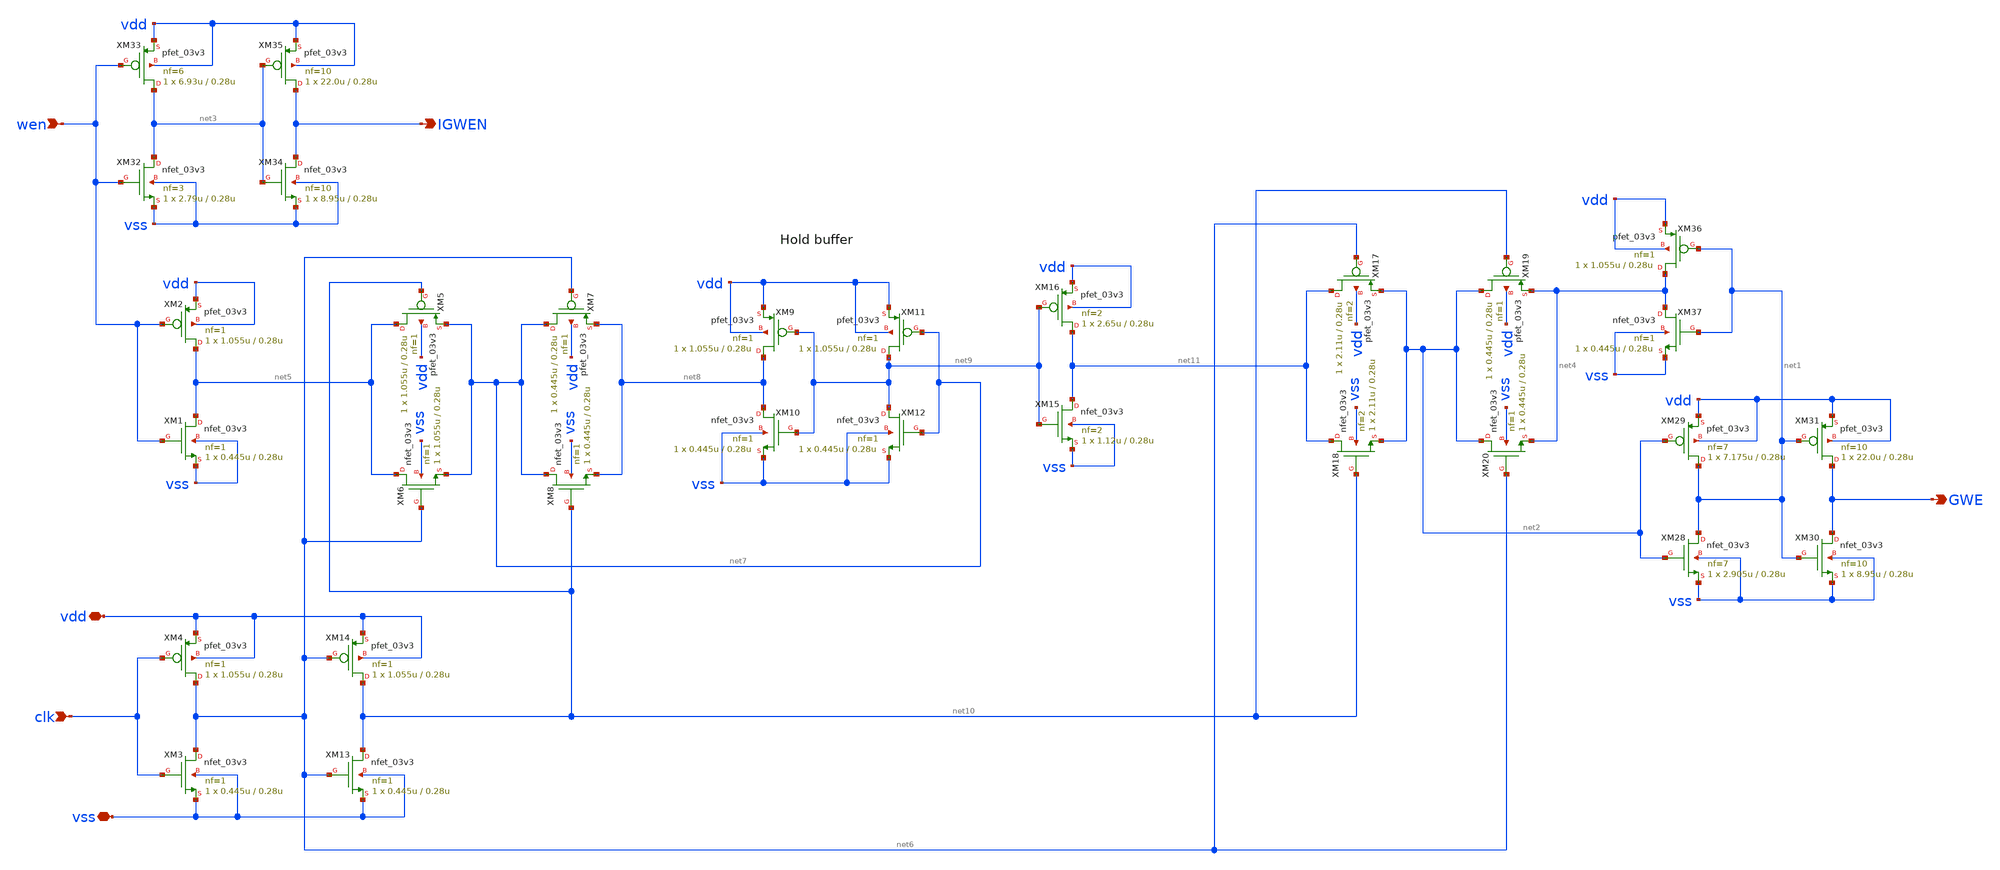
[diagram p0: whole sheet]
** sch_path: cells/gf180mcu_ocd_ip_sram__sram1024x8m8wm1/xschem/wen_v2_3v1024x8m81.sch
**.subckt wen_v2_3v1024x8m81 GWE wen IGWEN clk vdd vss
*.opin GWE
*.ipin wen
*.opin IGWEN
*.ipin clk
*.iopin vdd
*.iopin vss
XM28 net1 net2 vss vss nfet_03v3 L=0.28u W=2.905u nf=7 ad='int((nf+1)/2) * W/nf * 0.18u' as='int((nf+2)/2) * W/nf * 0.18u'
+ pd='2*int((nf+1)/2) * (W/nf + 0.18u)' ps='2*int((nf+2)/2) * (W/nf + 0.18u)' nrd='0.18u / W' nrs='0.18u / W'
+ sa=0 sb=0 sd=0 m=1
XM29 net1 net2 vdd vdd pfet_03v3 L=0.28u W=7.175u nf=7 ad='int((nf+1)/2) * W/nf * 0.18u' as='int((nf+2)/2) * W/nf * 0.18u'
+ pd='2*int((nf+1)/2) * (W/nf + 0.18u)' ps='2*int((nf+2)/2) * (W/nf + 0.18u)' nrd='0.18u / W' nrs='0.18u / W'
+ sa=0 sb=0 sd=0 m=1
XM30 GWE net1 vss vss nfet_03v3 L=0.28u W=8.95u nf=10 ad='int((nf+1)/2) * W/nf * 0.18u' as='int((nf+2)/2) * W/nf * 0.18u'
+ pd='2*int((nf+1)/2) * (W/nf + 0.18u)' ps='2*int((nf+2)/2) * (W/nf + 0.18u)' nrd='0.18u / W' nrs='0.18u / W'
+ sa=0 sb=0 sd=0 m=1
XM31 GWE net1 vdd vdd pfet_03v3 L=0.28u W=22.0u nf=10 ad='int((nf+1)/2) * W/nf * 0.18u' as='int((nf+2)/2) * W/nf * 0.18u'
+ pd='2*int((nf+1)/2) * (W/nf + 0.18u)' ps='2*int((nf+2)/2) * (W/nf + 0.18u)' nrd='0.18u / W' nrs='0.18u / W'
+ sa=0 sb=0 sd=0 m=1
XM32 net3 wen vss vss nfet_03v3 L=0.28u W=2.79u nf=3 ad='int((nf+1)/2) * W/nf * 0.18u' as='int((nf+2)/2) * W/nf * 0.18u'
+ pd='2*int((nf+1)/2) * (W/nf + 0.18u)' ps='2*int((nf+2)/2) * (W/nf + 0.18u)' nrd='0.18u / W' nrs='0.18u / W'
+ sa=0 sb=0 sd=0 m=1
XM33 net3 wen vdd vdd pfet_03v3 L=0.28u W=6.93u nf=6 ad='int((nf+1)/2) * W/nf * 0.18u' as='int((nf+2)/2) * W/nf * 0.18u'
+ pd='2*int((nf+1)/2) * (W/nf + 0.18u)' ps='2*int((nf+2)/2) * (W/nf + 0.18u)' nrd='0.18u / W' nrs='0.18u / W'
+ sa=0 sb=0 sd=0 m=1
XM34 IGWEN net3 vss vss nfet_03v3 L=0.28u W=8.95u nf=10 ad='int((nf+1)/2) * W/nf * 0.18u' as='int((nf+2)/2) * W/nf * 0.18u'
+ pd='2*int((nf+1)/2) * (W/nf + 0.18u)' ps='2*int((nf+2)/2) * (W/nf + 0.18u)' nrd='0.18u / W' nrs='0.18u / W'
+ sa=0 sb=0 sd=0 m=1
XM35 IGWEN net3 vdd vdd pfet_03v3 L=0.28u W=22.0u nf=10 ad='int((nf+1)/2) * W/nf * 0.18u' as='int((nf+2)/2) * W/nf * 0.18u'
+ pd='2*int((nf+1)/2) * (W/nf + 0.18u)' ps='2*int((nf+2)/2) * (W/nf + 0.18u)' nrd='0.18u / W' nrs='0.18u / W'
+ sa=0 sb=0 sd=0 m=1
XM36 net4 net1 vdd vdd pfet_03v3 L=0.28u W=1.055u nf=1 ad='int((nf+1)/2) * W/nf * 0.18u' as='int((nf+2)/2) * W/nf * 0.18u'
+ pd='2*int((nf+1)/2) * (W/nf + 0.18u)' ps='2*int((nf+2)/2) * (W/nf + 0.18u)' nrd='0.18u / W' nrs='0.18u / W'
+ sa=0 sb=0 sd=0 m=1
XM37 net4 net1 vss vss nfet_03v3 L=0.28u W=0.445u nf=1 ad='int((nf+1)/2) * W/nf * 0.18u' as='int((nf+2)/2) * W/nf * 0.18u'
+ pd='2*int((nf+1)/2) * (W/nf + 0.18u)' ps='2*int((nf+2)/2) * (W/nf + 0.18u)' nrd='0.18u / W' nrs='0.18u / W'
+ sa=0 sb=0 sd=0 m=1
XM1 net5 wen vss vss nfet_03v3 L=0.28u W=0.445u nf=1 ad='int((nf+1)/2) * W/nf * 0.18u' as='int((nf+2)/2) * W/nf * 0.18u'
+ pd='2*int((nf+1)/2) * (W/nf + 0.18u)' ps='2*int((nf+2)/2) * (W/nf + 0.18u)' nrd='0.18u / W' nrs='0.18u / W'
+ sa=0 sb=0 sd=0 m=1
XM2 net5 wen vdd vdd pfet_03v3 L=0.28u W=1.055u nf=1 ad='int((nf+1)/2) * W/nf * 0.18u' as='int((nf+2)/2) * W/nf * 0.18u'
+ pd='2*int((nf+1)/2) * (W/nf + 0.18u)' ps='2*int((nf+2)/2) * (W/nf + 0.18u)' nrd='0.18u / W' nrs='0.18u / W'
+ sa=0 sb=0 sd=0 m=1
XM3 net6 clk vss vss nfet_03v3 L=0.28u W=0.445u nf=1 ad='int((nf+1)/2) * W/nf * 0.18u' as='int((nf+2)/2) * W/nf * 0.18u'
+ pd='2*int((nf+1)/2) * (W/nf + 0.18u)' ps='2*int((nf+2)/2) * (W/nf + 0.18u)' nrd='0.18u / W' nrs='0.18u / W'
+ sa=0 sb=0 sd=0 m=1
XM4 net6 clk vdd vdd pfet_03v3 L=0.28u W=1.055u nf=1 ad='int((nf+1)/2) * W/nf * 0.18u' as='int((nf+2)/2) * W/nf * 0.18u'
+ pd='2*int((nf+1)/2) * (W/nf + 0.18u)' ps='2*int((nf+2)/2) * (W/nf + 0.18u)' nrd='0.18u / W' nrs='0.18u / W'
+ sa=0 sb=0 sd=0 m=1
XM5 net5 net10 net7 vdd pfet_03v3 L=0.28u W=1.055u nf=1 ad='int((nf+1)/2) * W/nf * 0.18u' as='int((nf+2)/2) * W/nf * 0.18u'
+ pd='2*int((nf+1)/2) * (W/nf + 0.18u)' ps='2*int((nf+2)/2) * (W/nf + 0.18u)' nrd='0.18u / W' nrs='0.18u / W'
+ sa=0 sb=0 sd=0 m=1
XM6 net5 net6 net7 vss nfet_03v3 L=0.28u W=1.055u nf=1 ad='int((nf+1)/2) * W/nf * 0.18u' as='int((nf+2)/2) * W/nf * 0.18u'
+ pd='2*int((nf+1)/2) * (W/nf + 0.18u)' ps='2*int((nf+2)/2) * (W/nf + 0.18u)' nrd='0.18u / W' nrs='0.18u / W'
+ sa=0 sb=0 sd=0 m=1
XM7 net7 net6 net8 vdd pfet_03v3 L=0.28u W=0.445u nf=1 ad='int((nf+1)/2) * W/nf * 0.18u' as='int((nf+2)/2) * W/nf * 0.18u'
+ pd='2*int((nf+1)/2) * (W/nf + 0.18u)' ps='2*int((nf+2)/2) * (W/nf + 0.18u)' nrd='0.18u / W' nrs='0.18u / W'
+ sa=0 sb=0 sd=0 m=1
XM8 net7 net10 net8 vss nfet_03v3 L=0.28u W=0.445u nf=1 ad='int((nf+1)/2) * W/nf * 0.18u' as='int((nf+2)/2) * W/nf * 0.18u'
+ pd='2*int((nf+1)/2) * (W/nf + 0.18u)' ps='2*int((nf+2)/2) * (W/nf + 0.18u)' nrd='0.18u / W' nrs='0.18u / W'
+ sa=0 sb=0 sd=0 m=1
XM9 net8 net9 vdd vdd pfet_03v3 L=0.28u W=1.055u nf=1 ad='int((nf+1)/2) * W/nf * 0.18u' as='int((nf+2)/2) * W/nf * 0.18u'
+ pd='2*int((nf+1)/2) * (W/nf + 0.18u)' ps='2*int((nf+2)/2) * (W/nf + 0.18u)' nrd='0.18u / W' nrs='0.18u / W'
+ sa=0 sb=0 sd=0 m=1
XM10 net8 net9 vss vss nfet_03v3 L=0.28u W=0.445u nf=1 ad='int((nf+1)/2) * W/nf * 0.18u' as='int((nf+2)/2) * W/nf * 0.18u'
+ pd='2*int((nf+1)/2) * (W/nf + 0.18u)' ps='2*int((nf+2)/2) * (W/nf + 0.18u)' nrd='0.18u / W' nrs='0.18u / W'
+ sa=0 sb=0 sd=0 m=1
XM11 net9 net7 vdd vdd pfet_03v3 L=0.28u W=1.055u nf=1 ad='int((nf+1)/2) * W/nf * 0.18u' as='int((nf+2)/2) * W/nf * 0.18u'
+ pd='2*int((nf+1)/2) * (W/nf + 0.18u)' ps='2*int((nf+2)/2) * (W/nf + 0.18u)' nrd='0.18u / W' nrs='0.18u / W'
+ sa=0 sb=0 sd=0 m=1
XM12 net9 net7 vss vss nfet_03v3 L=0.28u W=0.445u nf=1 ad='int((nf+1)/2) * W/nf * 0.18u' as='int((nf+2)/2) * W/nf * 0.18u'
+ pd='2*int((nf+1)/2) * (W/nf + 0.18u)' ps='2*int((nf+2)/2) * (W/nf + 0.18u)' nrd='0.18u / W' nrs='0.18u / W'
+ sa=0 sb=0 sd=0 m=1
XM13 net10 net6 vss vss nfet_03v3 L=0.28u W=0.445u nf=1 ad='int((nf+1)/2) * W/nf * 0.18u' as='int((nf+2)/2) * W/nf * 0.18u'
+ pd='2*int((nf+1)/2) * (W/nf + 0.18u)' ps='2*int((nf+2)/2) * (W/nf + 0.18u)' nrd='0.18u / W' nrs='0.18u / W'
+ sa=0 sb=0 sd=0 m=1
XM14 net10 net6 vdd vdd pfet_03v3 L=0.28u W=1.055u nf=1 ad='int((nf+1)/2) * W/nf * 0.18u' as='int((nf+2)/2) * W/nf * 0.18u'
+ pd='2*int((nf+1)/2) * (W/nf + 0.18u)' ps='2*int((nf+2)/2) * (W/nf + 0.18u)' nrd='0.18u / W' nrs='0.18u / W'
+ sa=0 sb=0 sd=0 m=1
XM15 net11 net9 vss vss nfet_03v3 L=0.28u W=1.12u nf=2 ad='int((nf+1)/2) * W/nf * 0.18u' as='int((nf+2)/2) * W/nf * 0.18u'
+ pd='2*int((nf+1)/2) * (W/nf + 0.18u)' ps='2*int((nf+2)/2) * (W/nf + 0.18u)' nrd='0.18u / W' nrs='0.18u / W'
+ sa=0 sb=0 sd=0 m=1
XM16 net11 net9 vdd vdd pfet_03v3 L=0.28u W=2.65u nf=2 ad='int((nf+1)/2) * W/nf * 0.18u' as='int((nf+2)/2) * W/nf * 0.18u'
+ pd='2*int((nf+1)/2) * (W/nf + 0.18u)' ps='2*int((nf+2)/2) * (W/nf + 0.18u)' nrd='0.18u / W' nrs='0.18u / W'
+ sa=0 sb=0 sd=0 m=1
XM17 net11 net6 net2 vdd pfet_03v3 L=0.28u W=2.11u nf=2 ad='int((nf+1)/2) * W/nf * 0.18u' as='int((nf+2)/2) * W/nf * 0.18u'
+ pd='2*int((nf+1)/2) * (W/nf + 0.18u)' ps='2*int((nf+2)/2) * (W/nf + 0.18u)' nrd='0.18u / W' nrs='0.18u / W'
+ sa=0 sb=0 sd=0 m=1
XM18 net11 net10 net2 vss nfet_03v3 L=0.28u W=2.11u nf=2 ad='int((nf+1)/2) * W/nf * 0.18u' as='int((nf+2)/2) * W/nf * 0.18u'
+ pd='2*int((nf+1)/2) * (W/nf + 0.18u)' ps='2*int((nf+2)/2) * (W/nf + 0.18u)' nrd='0.18u / W' nrs='0.18u / W'
+ sa=0 sb=0 sd=0 m=1
XM19 net2 net10 net4 vdd pfet_03v3 L=0.28u W=0.445u nf=1 ad='int((nf+1)/2) * W/nf * 0.18u' as='int((nf+2)/2) * W/nf * 0.18u'
+ pd='2*int((nf+1)/2) * (W/nf + 0.18u)' ps='2*int((nf+2)/2) * (W/nf + 0.18u)' nrd='0.18u / W' nrs='0.18u / W'
+ sa=0 sb=0 sd=0 m=1
XM20 net2 net6 net4 vss nfet_03v3 L=0.28u W=0.445u nf=1 ad='int((nf+1)/2) * W/nf * 0.18u' as='int((nf+2)/2) * W/nf * 0.18u'
+ pd='2*int((nf+1)/2) * (W/nf + 0.18u)' ps='2*int((nf+2)/2) * (W/nf + 0.18u)' nrd='0.18u / W' nrs='0.18u / W'
+ sa=0 sb=0 sd=0 m=1
**.ends
.end
